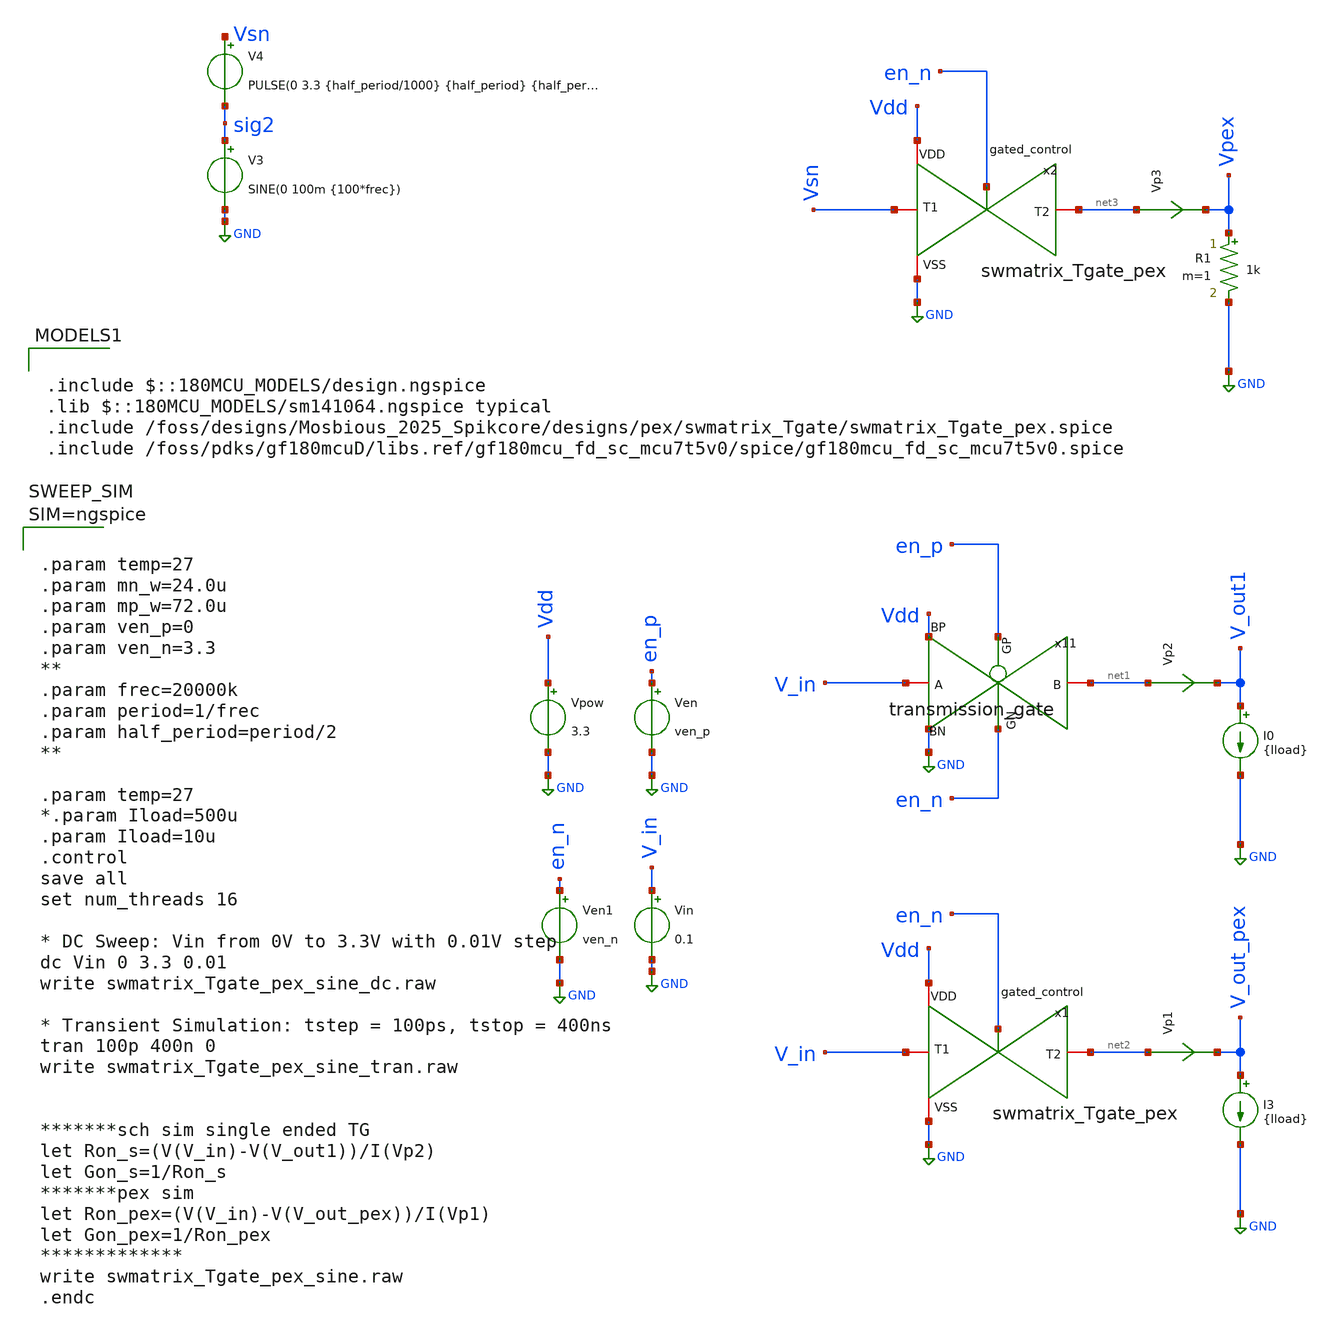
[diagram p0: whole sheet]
** sch_path: designs/pex/swmatrix_Tgate/swmatrix_Tgate_pex_sine_in.sch
**.subckt swmatrix_Tgate_pex_sine_in
Vpow Vdd GND 3.3
Vin V_in GND 0.1
Ven en_p GND ven_p
Ven1 en_n GND ven_n
I0 V_out1 GND {Iload}
Vp2 net1 V_out1 0
.save i(vp2)
x11 net1 en_n en_p V_in Vdd GND transmission_gate
x1 en_n net2 V_in GND Vdd swmatrix_Tgate_pex
I3 V_out_pex GND {Iload}
Vp1 net2 V_out_pex 0
.save i(vp1)
x2 en_n net3 Vsn GND Vdd swmatrix_Tgate_pex
Vp3 net3 Vpex 0
.save i(vp3)
R1 Vpex GND 1k m=1
V3 sig2 GND SINE(0 100m {100*frec})
V4 Vsn sig2 PULSE(0 3.3 {half_period/1000} {half_period} {half_period} {half_period/1000} {period})
**** begin user architecture code



.param temp=27
.param mn_w=24.0u
.param mp_w=72.0u
.param ven_p=0
.param ven_n=3.3
**
.param frec=20000k
.param period=1/frec
.param half_period=period/2
**

.param temp=27
*.param Iload=500u
.param Iload=10u
.control
save all
set num_threads 16

* DC Sweep: Vin from 0V to 3.3V with 0.01V step
dc Vin 0 3.3 0.01
write swmatrix_Tgate_pex_sine_dc.raw

* Transient Simulation: tstep = 100ps, tstop = 400ns
tran 100p 400n 0
write swmatrix_Tgate_pex_sine_tran.raw


*******sch sim single ended TG
let Ron_s=(V(V_in)-V(V_out1))/I(Vp2)
let Gon_s=1/Ron_s
*******pex sim
let Ron_pex=(V(V_in)-V(V_out_pex))/I(Vp1)
let Gon_pex=1/Ron_pex
*************
write swmatrix_Tgate_pex_sine.raw
.endc




.include $::180MCU_MODELS/design.ngspice
.lib $::180MCU_MODELS/sm141064.ngspice typical
.include /foss/designs/Mosbious_2025_Spikcore/designs/pex/swmatrix_Tgate/swmatrix_Tgate_pex.spice
.include /foss/pdks/gf180mcuD/libs.ref/gf180mcu_fd_sc_mcu7t5v0/spice/gf180mcu_fd_sc_mcu7t5v0.spice

**** end user architecture code
**.ends

* expanding   symbol:  designs/libs/switch_matrix_gf180mcu_9t5v0/tgate_PK/transmission_gate.sym # of
*+ pins=6
** sym_path: designs/libs/switch_matrix_gf180mcu_9t5v0/tgate_PK/transmission_gate.sym
** sch_path: designs/libs/switch_matrix_gf180mcu_9t5v0/tgate_PK/transmission_gate.sch
.subckt transmission_gate B GN GP A BP BN
*.iopin B
*.iopin GN
*.iopin A
*.iopin GP
*.iopin BN
*.iopin BP
XM1 A GN B BN nfet_03v3 L=0.28u W=mn_w nf=6 ad='int((nf+1)/2) * W/nf * 0.18u' as='int((nf+2)/2) * W/nf * 0.18u'
+ pd='2*int((nf+1)/2) * (W/nf + 0.18u)' ps='2*int((nf+2)/2) * (W/nf + 0.18u)' nrd='0.18u / W' nrs='0.18u / W'
+ sa=0 sb=0 sd=0 m=1
XM2 A GP B BP pfet_03v3 L=0.28u W=mp_w nf=6 ad='int((nf+1)/2) * W/nf * 0.18u' as='int((nf+2)/2) * W/nf * 0.18u'
+ pd='2*int((nf+1)/2) * (W/nf + 0.18u)' ps='2*int((nf+2)/2) * (W/nf + 0.18u)' nrd='0.18u / W' nrs='0.18u / W'
+ sa=0 sb=0 sd=0 m=1
.ends

.GLOBAL GND
.end
